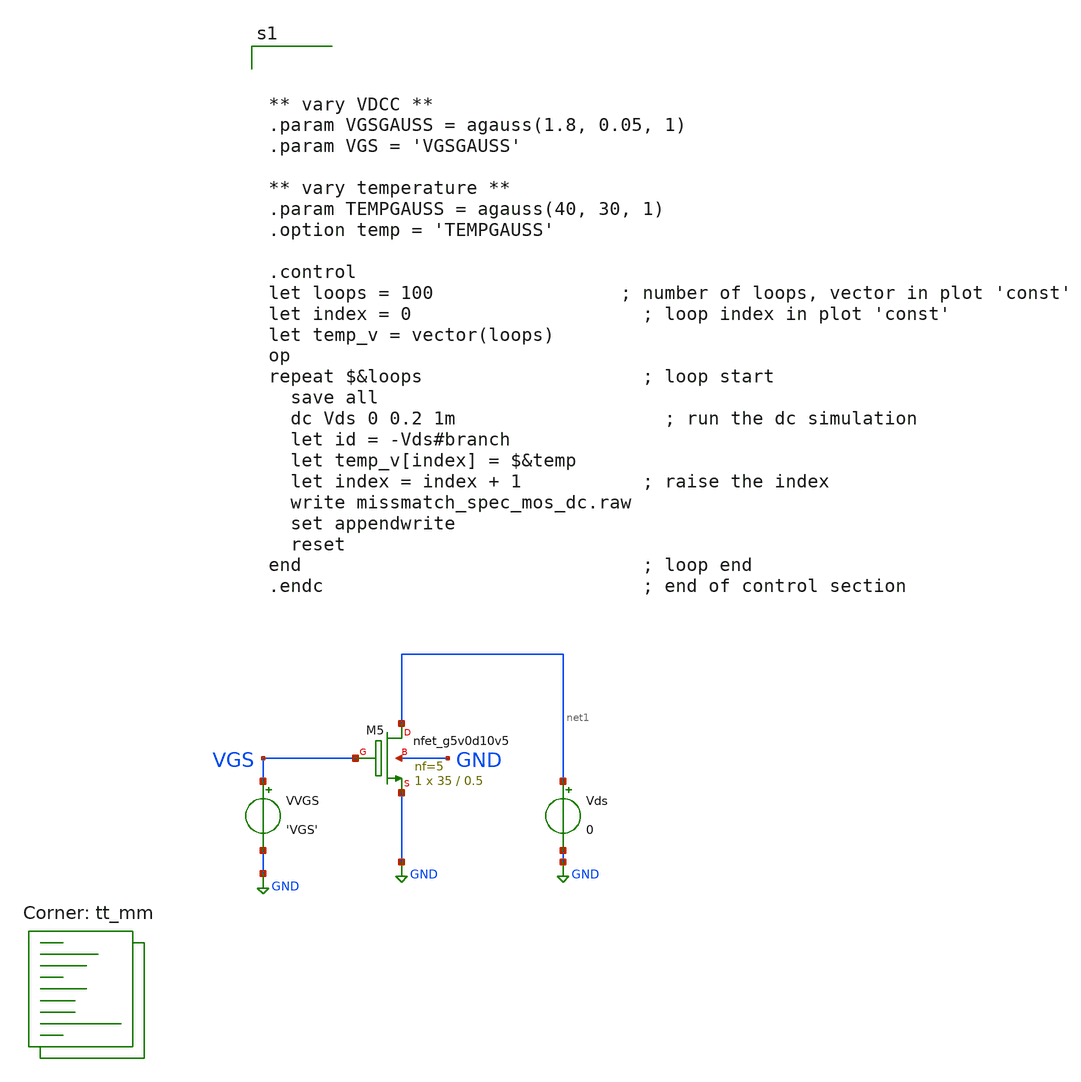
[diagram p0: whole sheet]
** sch_path: xschem/missmatch_spec_mos_dc.sch
**.subckt missmatch_spec_mos_dc
XM5 net1 VGS GND GND sky130_fd_pr__nfet_g5v0d10v5 L=0.5 W=35 nf=5 ad='int((5 + 1)/2) * 35 / 5 * 0.29'
+ as='int((5 + 2)/2) * 35 / 5 * 0.29' pd='2*int((5 + 1)/2) * (35 / 5 + 0.29)' ps='2*int((5 + 2)/2) * (35 / 5 + 0.29)'
+ nrd='0.29 / 35 ' nrs='0.29 / 35 ' sa=0 sb=0 sd=0 mult=1 m=1
VVGS VGS GND 'VGS'
Vds net1 GND 0
**** begin user architecture code
.lib $::SKYWATER_MODELS/sky130.lib.spice tt_mm



** vary VDCC **
.param VGSGAUSS = agauss(1.8, 0.05, 1)
.param VGS = 'VGSGAUSS'

** vary temperature **
.param TEMPGAUSS = agauss(40, 30, 1)
.option temp = 'TEMPGAUSS'

.control
let loops = 100                 ; number of loops, vector in plot 'const'
let index = 0                     ; loop index in plot 'const'
let temp_v = vector(loops)
op
repeat $&loops                    ; loop start
  save all
  dc Vds 0 0.2 1m                   ; run the dc simulation
  let id = -Vds#branch
  let temp_v[index] = $&temp
  let index = index + 1           ; raise the index
  write missmatch_spec_mos_dc.raw
  set appendwrite
  reset
end                               ; loop end
.endc                             ; end of control section


**** end user architecture code
**.ends
.GLOBAL GND
.end
